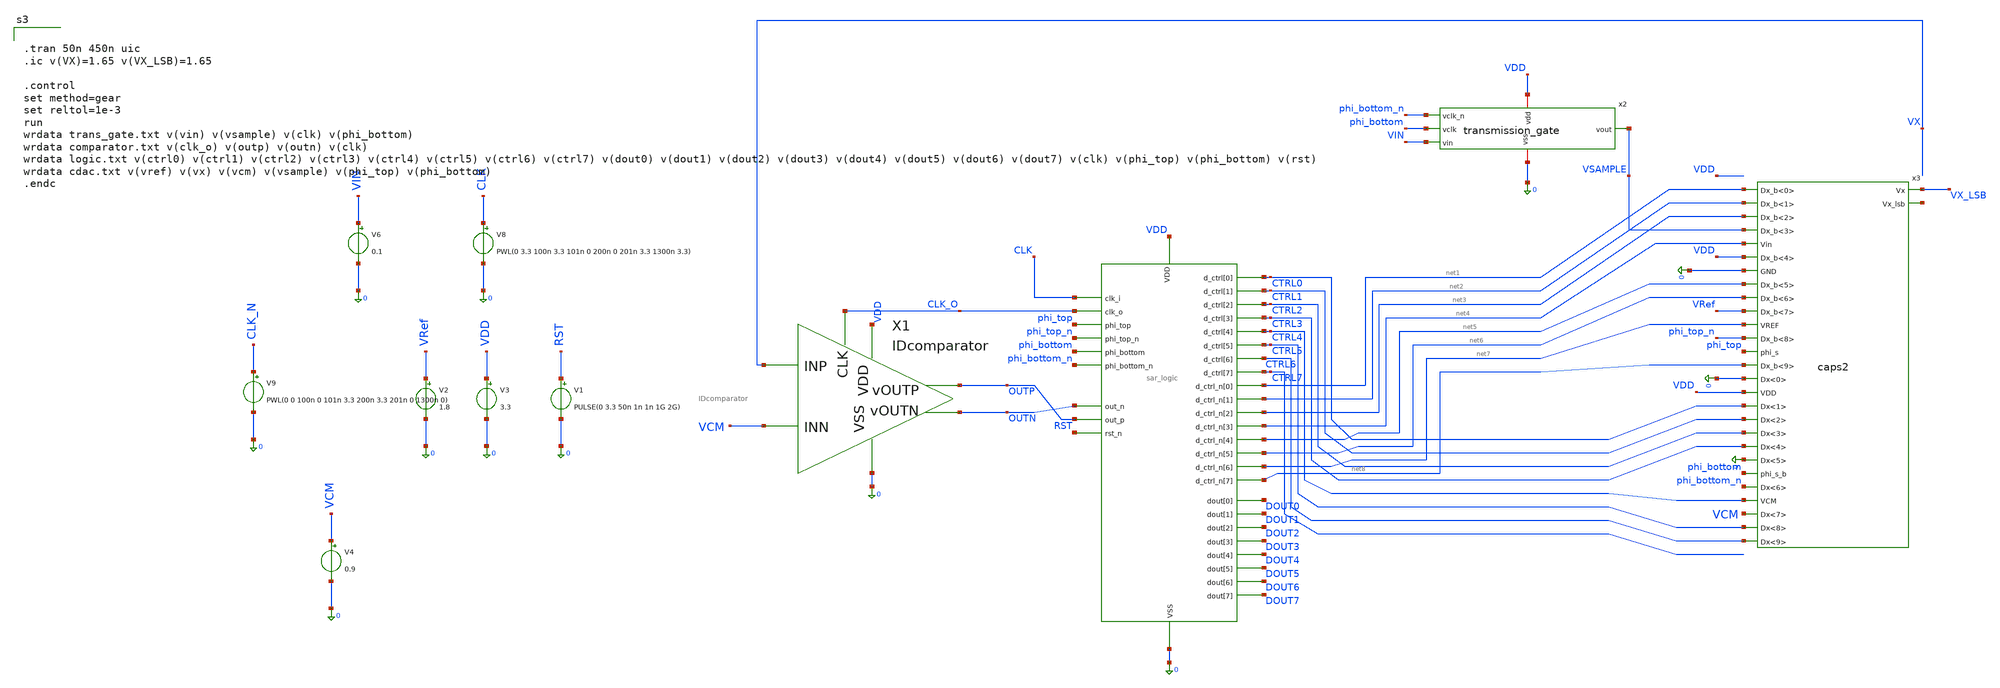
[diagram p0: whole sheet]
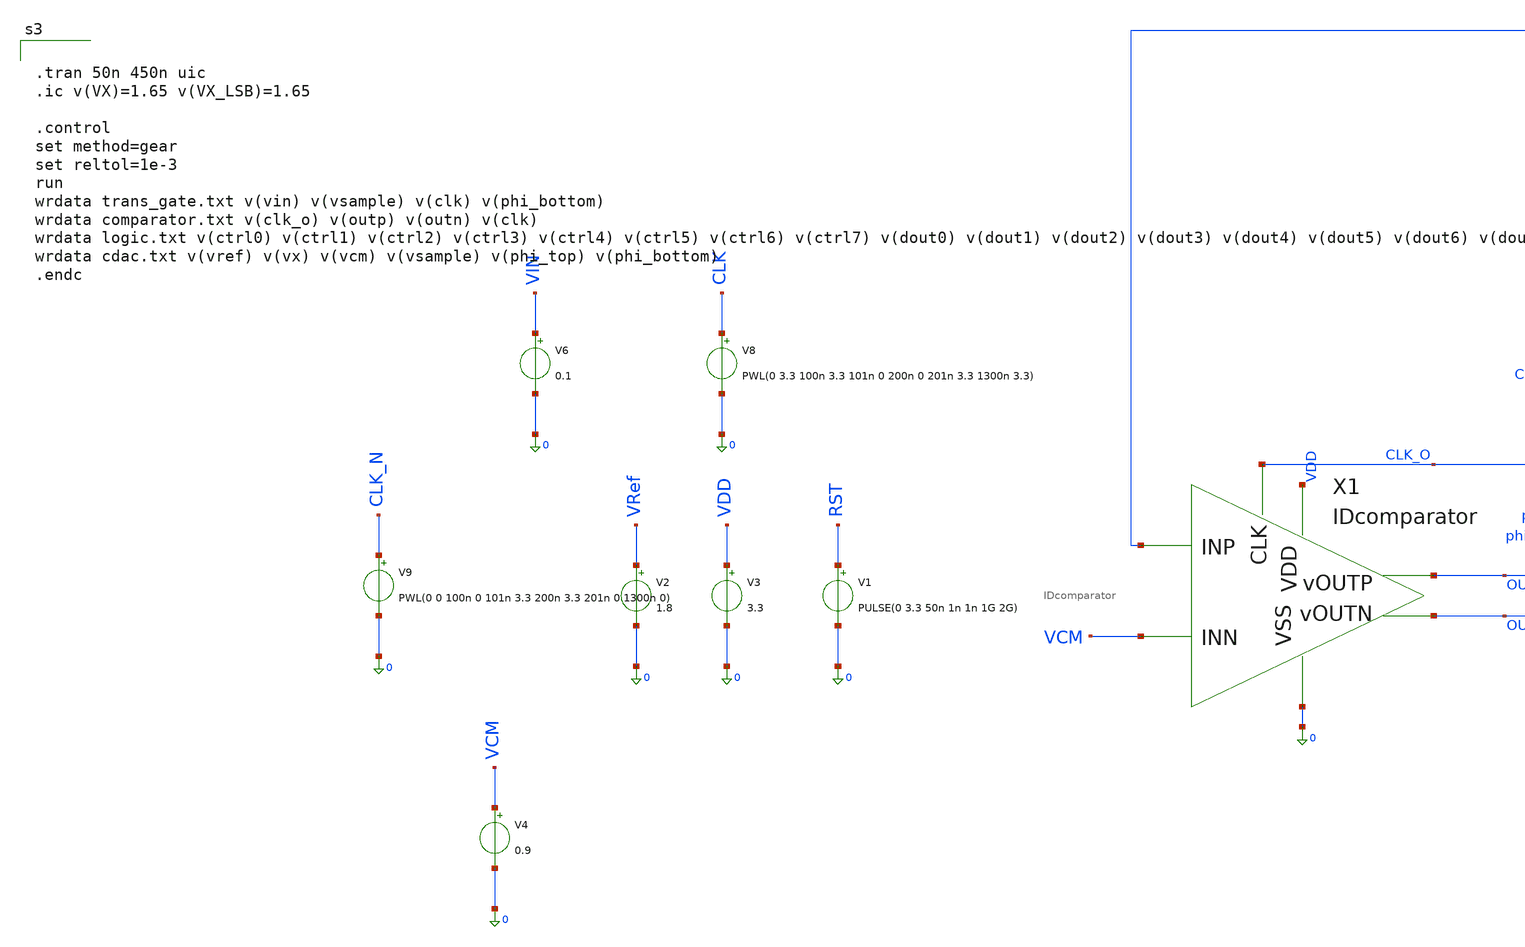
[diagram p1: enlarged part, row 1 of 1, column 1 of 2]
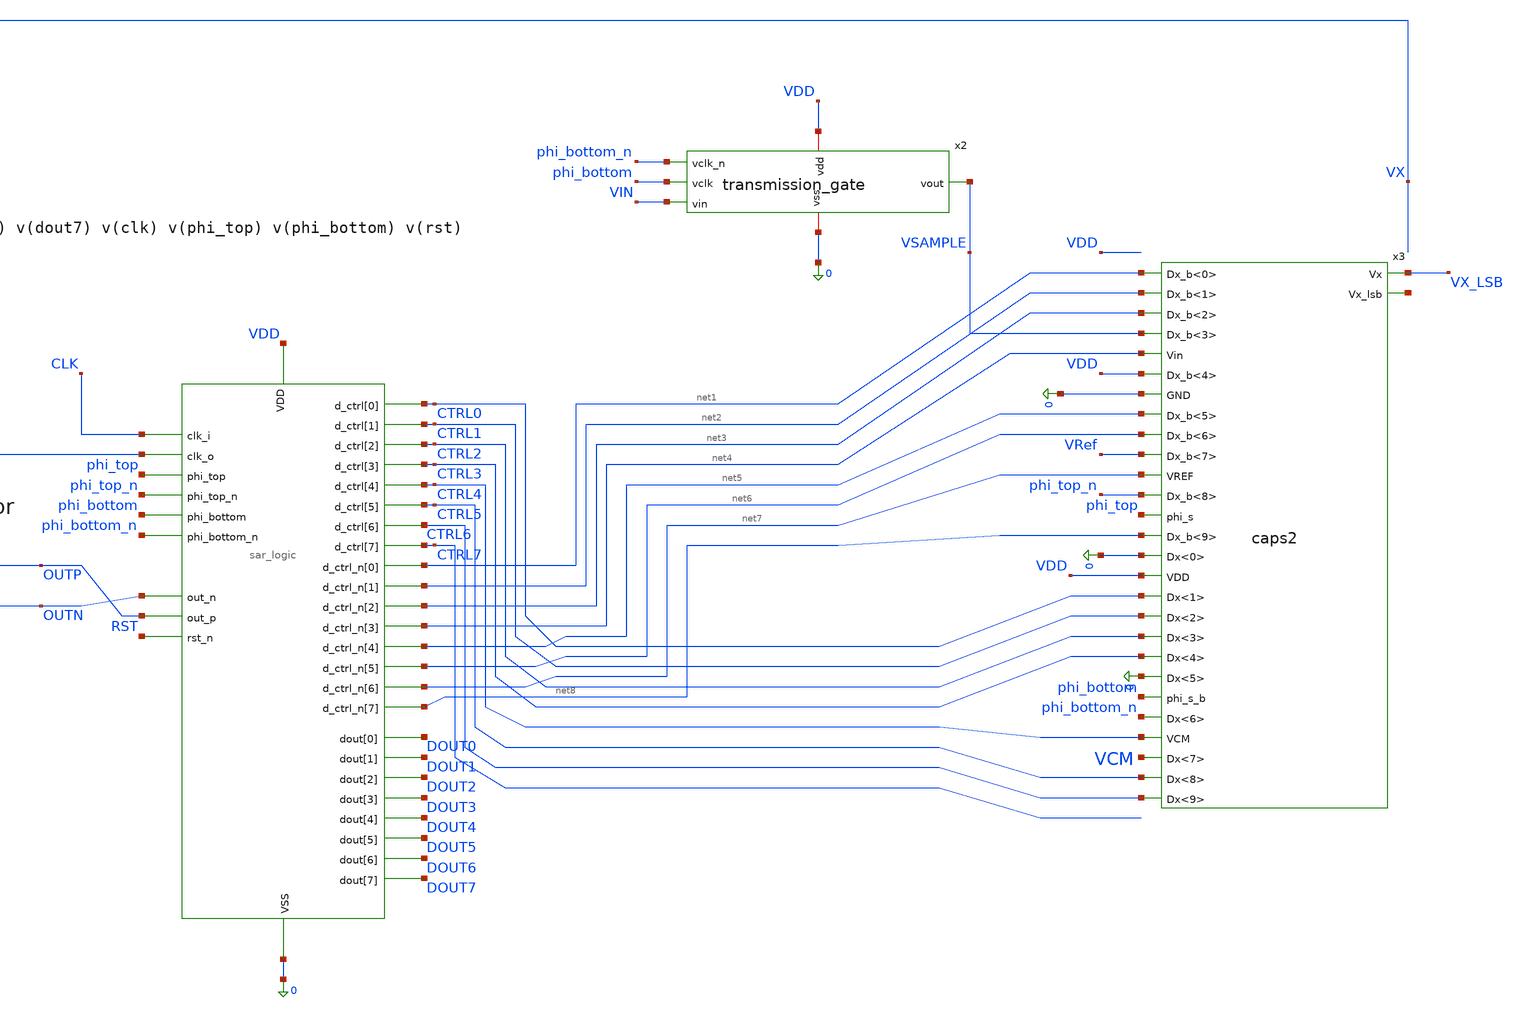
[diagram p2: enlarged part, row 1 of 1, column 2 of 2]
** sch_path: analog/top/top.sch
**.subckt top
V8 CLK 0 PWL(0 3.3 100n 3.3 101n 0 200n 0 201n 3.3 1300n 3.3)
V3 VDD 0 3.3
V1 RST 0 PULSE(0 3.3 50n 1n 1n 1G 2G)
V6 VIN 0 0.1
V2 VRef 0 1.8
V9 CLK_N 0 PWL(0 0 100n 0 101n 3.3 200n 3.3 201n 0 1300n 0)
V4 VCM 0 0.9
x2 VDD VSAMPLE phi_bottom_n phi_bottom VIN 0 transmission_gate
x3 net1 net2 net3 VSAMPLE net4 VDD 0 net5 net6 VRef net7 phi_top_n phi_top net8 0 VDD CTRL0 VX_LSB
+ CTRL1 CTRL2 net9 CTRL3 0 phi_bottom phi_bottom_n CTRL4 VCM CTRL5 CTRL6 caps2
X4 VDD 0 CLK_O CTRL0 CTRL1 CTRL2 CTRL3 CTRL4 CTRL5 CTRL6 CTRL7 DOUT0 DOUT2 DOUT3 DOUT4 DOUT5 DOUT6
+ DOUT7 OUTN OUTP RST phi_top phi_top_n phi_bottom phi_bottom_n CLK DOUT1 net1 net2 net3 net4 net5 net6
+ net7 net8 sar_adc_logic
X1 VX VCM CLK_O VDD 0 OUTP OUTN IDcomparator
**** begin user architecture code


.include /foss/designs/chipathon-2026-ti-adc/analog/digital/SAR_ADC_LOGIC/sar_adc_logic.spice
.include /foss/designs/chipathon-2026-ti-adc/analog/blocks/IDcomparator/IDcomparator.spice



.include $::180MCU_MODELS/design.ngspice
.include $PDK_ROOT/gf180mcuD/libs.ref/gf180mcu_fd_sc_mcu7t5v0/spice/gf180mcu_fd_sc_mcu7t5v0.spice
.lib $::180MCU_MODELS/sm141064.ngspice typical
.lib $::180MCU_MODELS/smbb000149.ngspice typical
.lib /foss/pdks/gf180mcuD/libs.tech/ngspice/sm141064.ngspice cap_mim
.lib /foss/pdks/gf180mcuD/libs.tech/ngspice/sm141064.ngspice mimcap_typical



.tran 50n 450n uic
.ic v(VX)=1.65 v(VX_LSB)=1.65

.control
set method=gear
set reltol=1e-3
run
wrdata trans_gate.txt v(vin) v(vsample) v(clk) v(phi_bottom)
wrdata comparator.txt v(clk_o) v(outp) v(outn) v(clk)
wrdata logic.txt v(ctrl0) v(ctrl1) v(ctrl2) v(ctrl3) v(ctrl4) v(ctrl5) v(ctrl6) v(ctrl7) v(dout0)
+ v(dout1) v(dout2) v(dout3) v(dout4) v(dout5) v(dout6) v(dout7) v(clk) v(phi_top) v(phi_bottom) v(rst)
wrdata cdac.txt v(vref) v(vx) v(vcm) v(vsample) v(phi_top) v(phi_bottom)
.endc


**** end user architecture code
**.ends
.end
